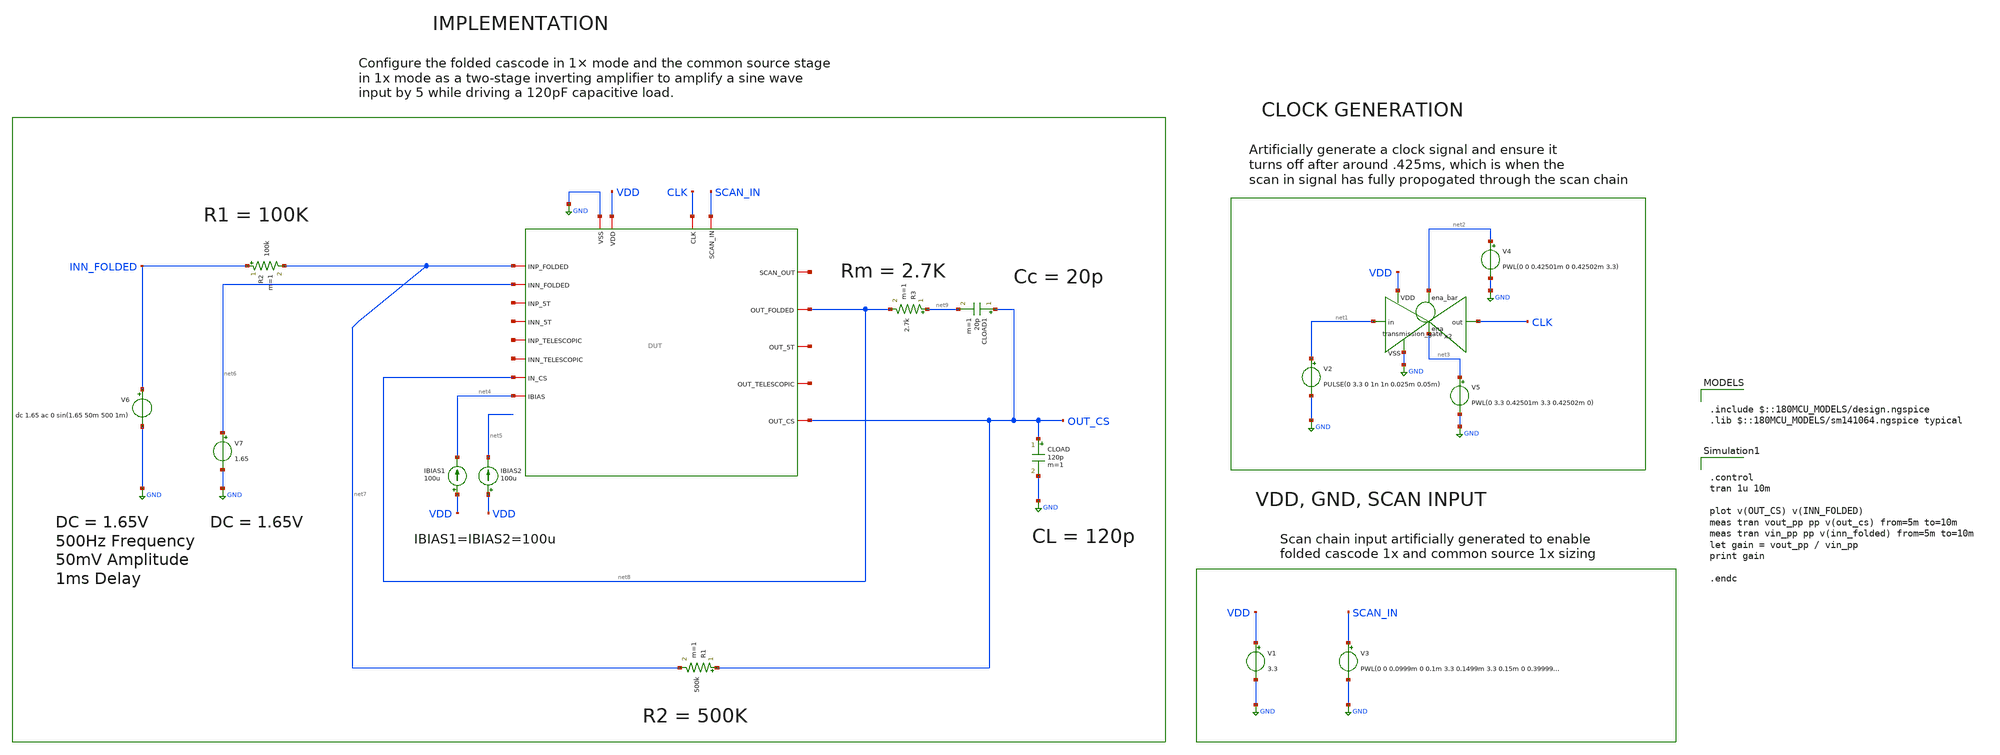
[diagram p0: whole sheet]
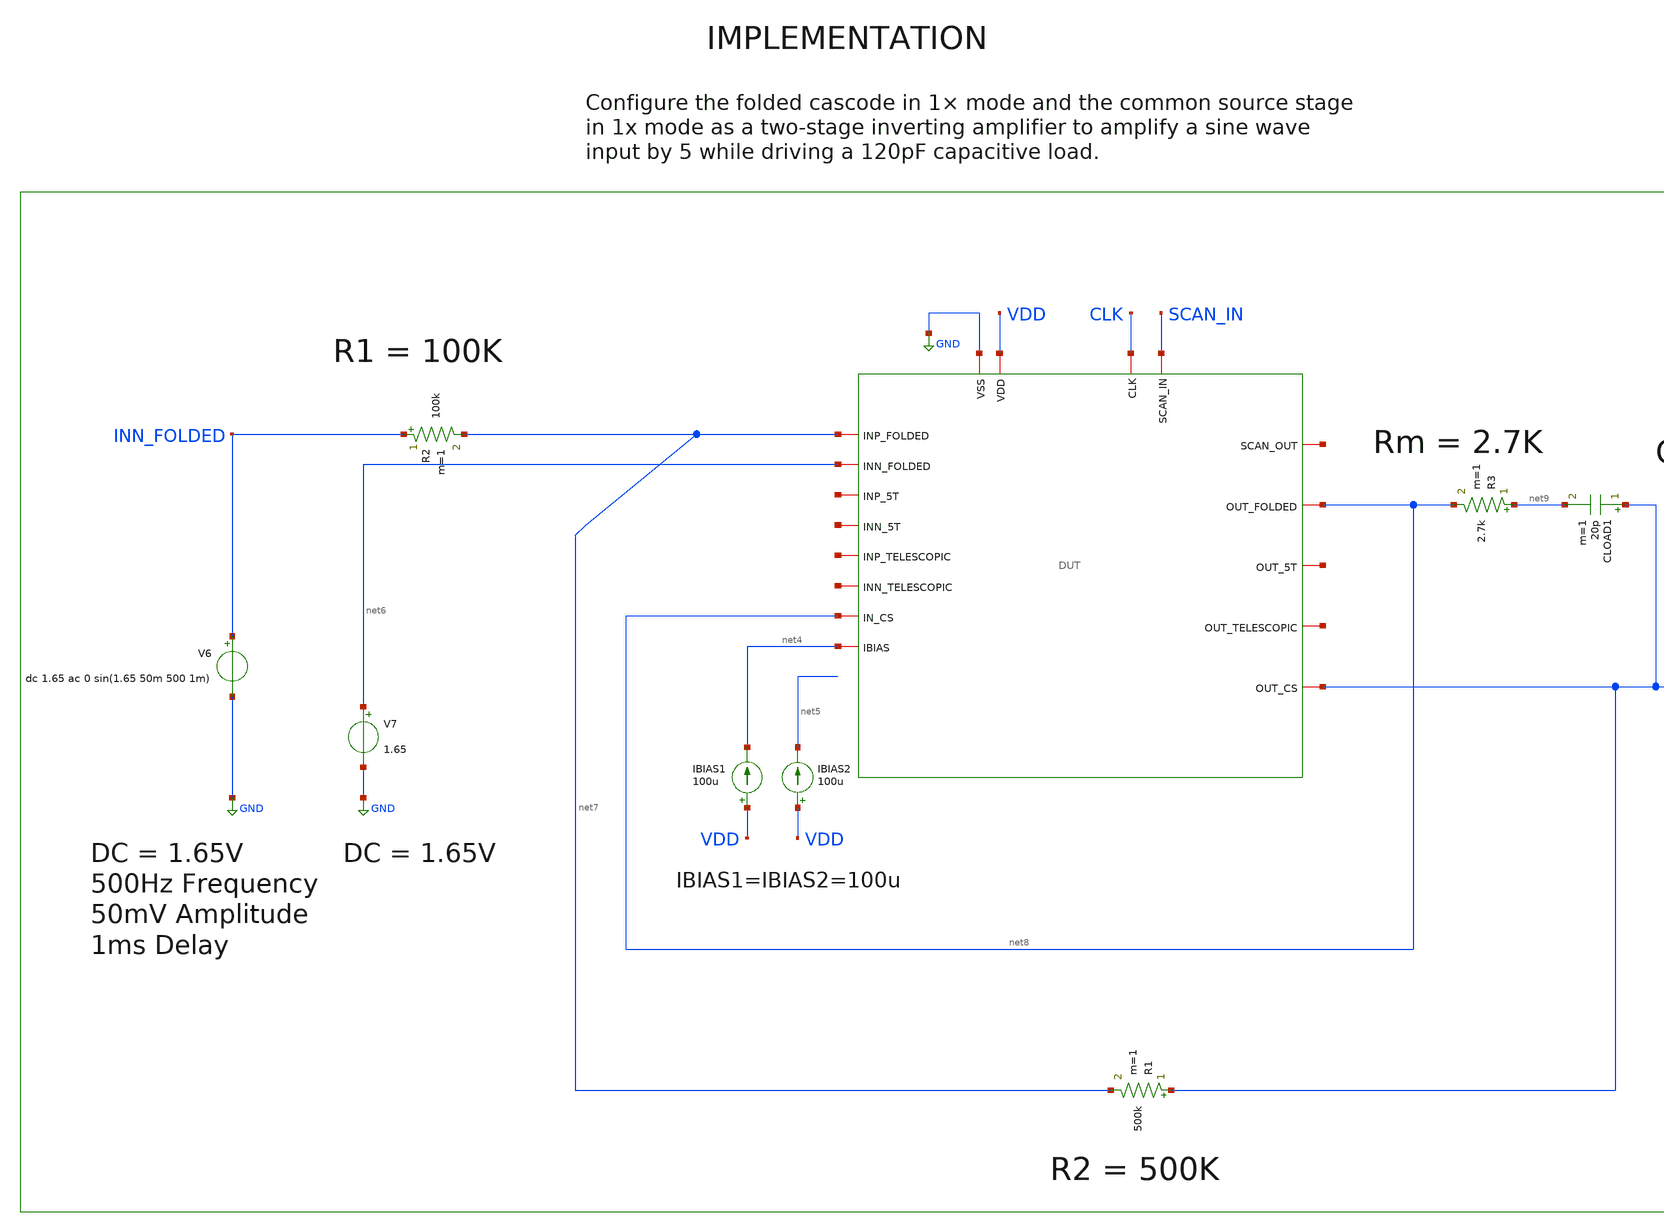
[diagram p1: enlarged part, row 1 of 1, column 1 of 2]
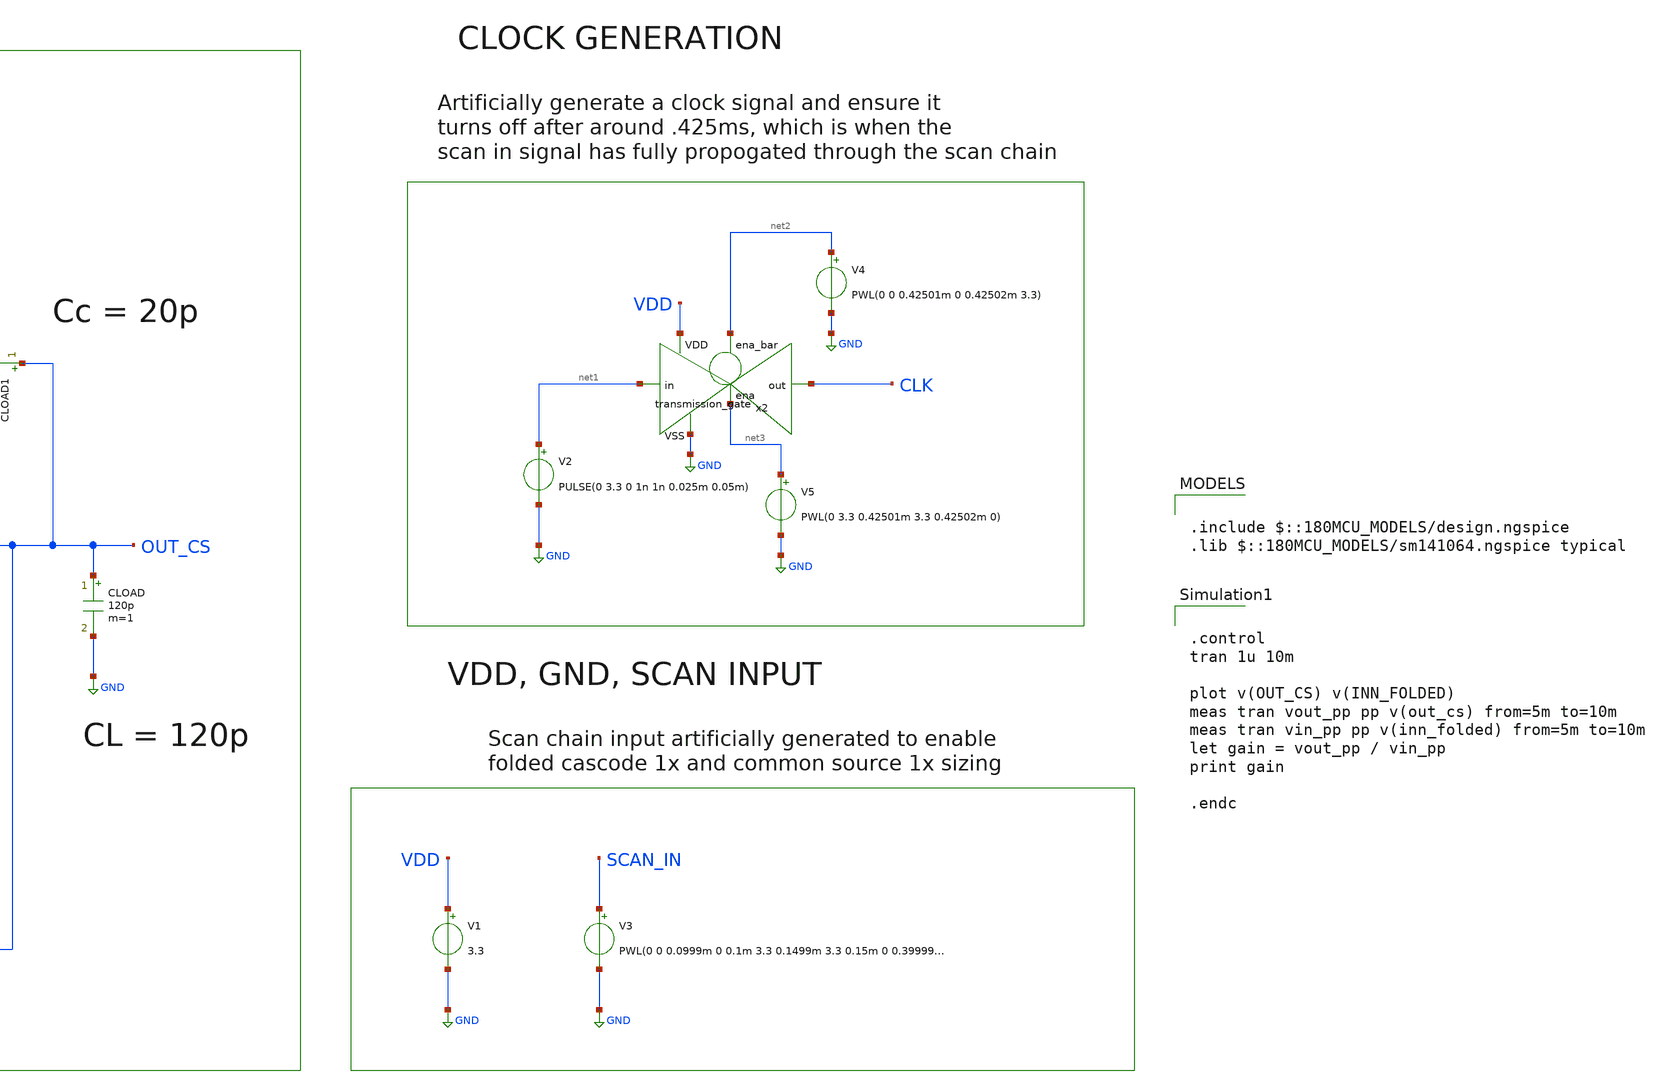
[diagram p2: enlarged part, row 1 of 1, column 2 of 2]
** sch_path: designs/libs/core_tb/etj/ota_folded/two_stage/inverting_amp.sch
**.subckt inverting_amp
V3 SCAN_IN GND PWL(0 0 0.0999m 0 0.1m 3.3 0.1499m 3.3 0.15m 0 0.39999m 0 0.4m 3.3 0.499999m 3.3 0.5m
+ 0)
V1 VDD GND 3.3
V2 net1 GND PULSE(0 3.3 0 1n 1n 0.025m 0.05m)
x2 net2 VDD CLK net1 GND net3 transmission_gate
V4 net2 GND PWL(0 0 0.42501m 0 0.42502m 3.3)
V5 net3 GND PWL(0 3.3 0.42501m 3.3 0.42502m 0)
IBIAS1 VDD net4 100u
IBIAS2 VDD net5 100u
CLOAD OUT_CS GND 120p m=1
R3 net9 net8 2.7k m=1
CLOAD1 OUT_CS net9 20p m=1
V7 net6 GND 1.65
x1 CLK net10 SCAN_IN GND VDD net8 net7 net11 net4 net6 net12 net13 net14 net15 OUT_CS net8 net16 DUT
R2 INN_FOLDED net7 100k m=1
R1 OUT_CS net7 500k m=1
V6 INN_FOLDED GND dc 1.65 ac 0 sin(1.65 50m 500 1m)
**** begin user architecture code

.include $::180MCU_MODELS/design.ngspice
.lib $::180MCU_MODELS/sm141064.ngspice typical



.control
tran 1u 10m

plot v(OUT_CS) v(INN_FOLDED)
meas tran vout_pp pp v(out_cs) from=5m to=10m
meas tran vin_pp pp v(inn_folded) from=5m to=10m
let gain = vout_pp / vin_pp
print gain

.endc


**** end user architecture code
**.ends
.GLOBAL GND
.end
